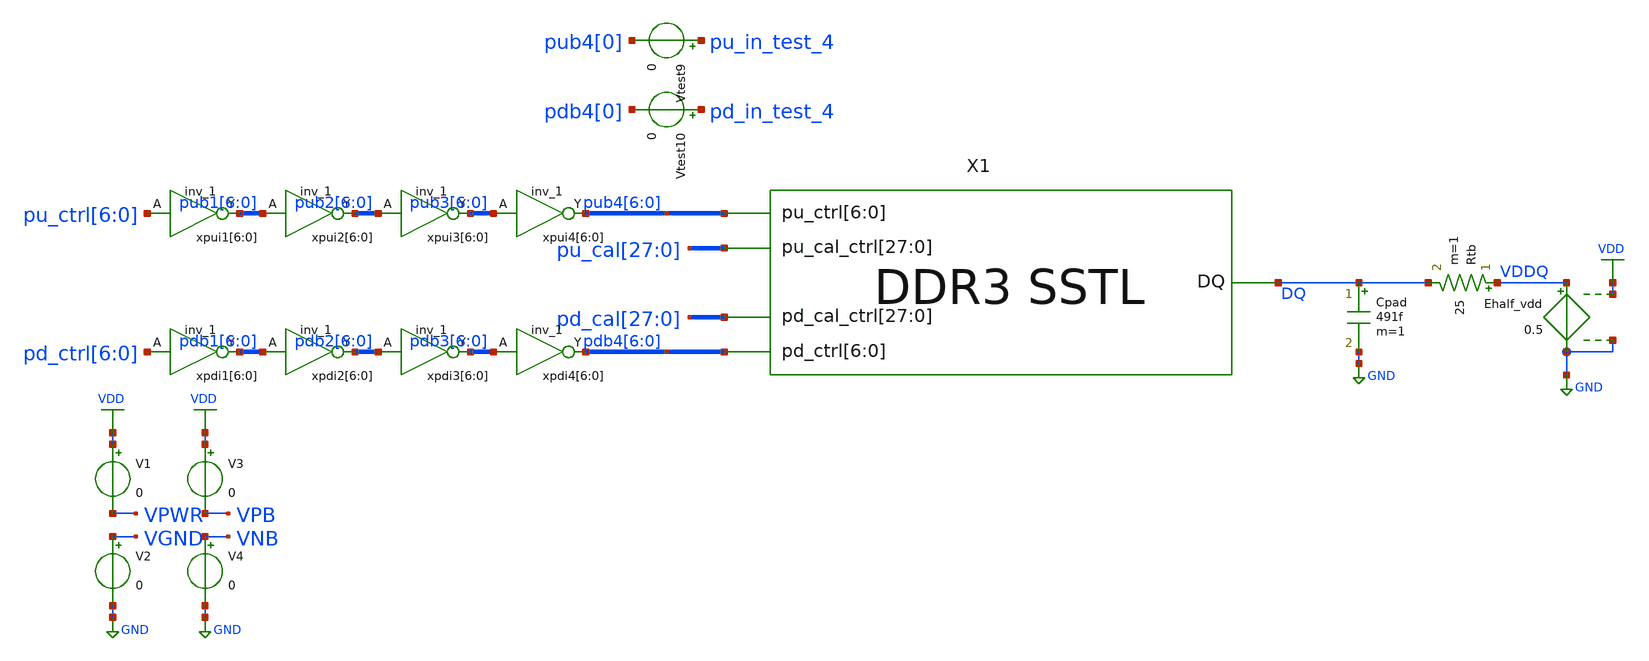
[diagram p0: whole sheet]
** sch_path: sstl_slew_tb.sch
* Copyright 2021 Stefan Frederik Schippers
* Licensed under the Apache License, Version 2.0 (the "License");
* you may not use this file except in compliance with the License.
* You may obtain a copy of the License at
* https://www.apache.org/licenses/LICENSE-2.0
* Unless required by applicable law or agreed to in writing, software
* distributed under the License is distributed on an "AS IS" BASIS,
* WITHOUT WARRANTIES OR CONDITIONS OF ANY KIND, either express or implied.
* See the License for the specific language governing permissions and
* limitations under the License.
**.subckt sstl_slew_tb
X1 DQ pdb4[6] pdb4[5] pdb4[4] pdb4[3] pdb4[2] pdb4[1] pdb4[0] pub4[6] pub4[5] pub4[4] pub4[3]
+ pub4[2] pub4[1] pub4[0] pd_cal[27] pd_cal[26] pd_cal[25] pd_cal[24] pd_cal[23] pd_cal[22] pd_cal[21]
+ pd_cal[20] pd_cal[19] pd_cal[18] pd_cal[17] pd_cal[16] pd_cal[15] pd_cal[14] pd_cal[13] pd_cal[12] pd_cal[11]
+ pd_cal[10] pd_cal[9] pd_cal[8] pd_cal[7] pd_cal[6] pd_cal[5] pd_cal[4] pd_cal[3] pd_cal[2] pd_cal[1] pd_cal[0]
+ pu_cal[27] pu_cal[26] pu_cal[25] pu_cal[24] pu_cal[23] pu_cal[22] pu_cal[21] pu_cal[20] pu_cal[19] pu_cal[18]
+ pu_cal[17] pu_cal[16] pu_cal[15] pu_cal[14] pu_cal[13] pu_cal[12] pu_cal[11] pu_cal[10] pu_cal[9] pu_cal[8]
+ pu_cal[7] pu_cal[6] pu_cal[5] pu_cal[4] pu_cal[3] pu_cal[2] pu_cal[1] pu_cal[0] SSTL
Rtb VDDQ DQ 25 m=1
Cpad DQ GND 491f m=1
Ehalf_vdd VDDQ GND VDD GND 0.5
xpui1[6] pu_ctrl[6] VGND VNB VPB VPWR pub1[6] sky130_fd_sc_hd__inv_1
xpui1[5] pu_ctrl[5] VGND VNB VPB VPWR pub1[5] sky130_fd_sc_hd__inv_1
xpui1[4] pu_ctrl[4] VGND VNB VPB VPWR pub1[4] sky130_fd_sc_hd__inv_1
xpui1[3] pu_ctrl[3] VGND VNB VPB VPWR pub1[3] sky130_fd_sc_hd__inv_1
xpui1[2] pu_ctrl[2] VGND VNB VPB VPWR pub1[2] sky130_fd_sc_hd__inv_1
xpui1[1] pu_ctrl[1] VGND VNB VPB VPWR pub1[1] sky130_fd_sc_hd__inv_1
xpui1[0] pu_ctrl[0] VGND VNB VPB VPWR pub1[0] sky130_fd_sc_hd__inv_1
xpui2[6] pub1[6] VGND VNB VPB VPWR pub2[6] sky130_fd_sc_hd__inv_1
xpui2[5] pub1[5] VGND VNB VPB VPWR pub2[5] sky130_fd_sc_hd__inv_1
xpui2[4] pub1[4] VGND VNB VPB VPWR pub2[4] sky130_fd_sc_hd__inv_1
xpui2[3] pub1[3] VGND VNB VPB VPWR pub2[3] sky130_fd_sc_hd__inv_1
xpui2[2] pub1[2] VGND VNB VPB VPWR pub2[2] sky130_fd_sc_hd__inv_1
xpui2[1] pub1[1] VGND VNB VPB VPWR pub2[1] sky130_fd_sc_hd__inv_1
xpui2[0] pub1[0] VGND VNB VPB VPWR pub2[0] sky130_fd_sc_hd__inv_1
xpui3[6] pub2[6] VGND VNB VPB VPWR pub3[6] sky130_fd_sc_hd__inv_1
xpui3[5] pub2[5] VGND VNB VPB VPWR pub3[5] sky130_fd_sc_hd__inv_1
xpui3[4] pub2[4] VGND VNB VPB VPWR pub3[4] sky130_fd_sc_hd__inv_1
xpui3[3] pub2[3] VGND VNB VPB VPWR pub3[3] sky130_fd_sc_hd__inv_1
xpui3[2] pub2[2] VGND VNB VPB VPWR pub3[2] sky130_fd_sc_hd__inv_1
xpui3[1] pub2[1] VGND VNB VPB VPWR pub3[1] sky130_fd_sc_hd__inv_1
xpui3[0] pub2[0] VGND VNB VPB VPWR pub3[0] sky130_fd_sc_hd__inv_1
xpui4[6] pub3[6] VGND VNB VPB VPWR pub4[6] sky130_fd_sc_hd__inv_1
xpui4[5] pub3[5] VGND VNB VPB VPWR pub4[5] sky130_fd_sc_hd__inv_1
xpui4[4] pub3[4] VGND VNB VPB VPWR pub4[4] sky130_fd_sc_hd__inv_1
xpui4[3] pub3[3] VGND VNB VPB VPWR pub4[3] sky130_fd_sc_hd__inv_1
xpui4[2] pub3[2] VGND VNB VPB VPWR pub4[2] sky130_fd_sc_hd__inv_1
xpui4[1] pub3[1] VGND VNB VPB VPWR pub4[1] sky130_fd_sc_hd__inv_1
xpui4[0] pub3[0] VGND VNB VPB VPWR pub4[0] sky130_fd_sc_hd__inv_1
xpdi1[6] pd_ctrl[6] VGND VNB VPB VPWR pdb1[6] sky130_fd_sc_hd__inv_1
xpdi1[5] pd_ctrl[5] VGND VNB VPB VPWR pdb1[5] sky130_fd_sc_hd__inv_1
xpdi1[4] pd_ctrl[4] VGND VNB VPB VPWR pdb1[4] sky130_fd_sc_hd__inv_1
xpdi1[3] pd_ctrl[3] VGND VNB VPB VPWR pdb1[3] sky130_fd_sc_hd__inv_1
xpdi1[2] pd_ctrl[2] VGND VNB VPB VPWR pdb1[2] sky130_fd_sc_hd__inv_1
xpdi1[1] pd_ctrl[1] VGND VNB VPB VPWR pdb1[1] sky130_fd_sc_hd__inv_1
xpdi1[0] pd_ctrl[0] VGND VNB VPB VPWR pdb1[0] sky130_fd_sc_hd__inv_1
xpdi2[6] pdb1[6] VGND VNB VPB VPWR pdb2[6] sky130_fd_sc_hd__inv_1
xpdi2[5] pdb1[5] VGND VNB VPB VPWR pdb2[5] sky130_fd_sc_hd__inv_1
xpdi2[4] pdb1[4] VGND VNB VPB VPWR pdb2[4] sky130_fd_sc_hd__inv_1
xpdi2[3] pdb1[3] VGND VNB VPB VPWR pdb2[3] sky130_fd_sc_hd__inv_1
xpdi2[2] pdb1[2] VGND VNB VPB VPWR pdb2[2] sky130_fd_sc_hd__inv_1
xpdi2[1] pdb1[1] VGND VNB VPB VPWR pdb2[1] sky130_fd_sc_hd__inv_1
xpdi2[0] pdb1[0] VGND VNB VPB VPWR pdb2[0] sky130_fd_sc_hd__inv_1
xpdi3[6] pdb2[6] VGND VNB VPB VPWR pdb3[6] sky130_fd_sc_hd__inv_1
xpdi3[5] pdb2[5] VGND VNB VPB VPWR pdb3[5] sky130_fd_sc_hd__inv_1
xpdi3[4] pdb2[4] VGND VNB VPB VPWR pdb3[4] sky130_fd_sc_hd__inv_1
xpdi3[3] pdb2[3] VGND VNB VPB VPWR pdb3[3] sky130_fd_sc_hd__inv_1
xpdi3[2] pdb2[2] VGND VNB VPB VPWR pdb3[2] sky130_fd_sc_hd__inv_1
xpdi3[1] pdb2[1] VGND VNB VPB VPWR pdb3[1] sky130_fd_sc_hd__inv_1
xpdi3[0] pdb2[0] VGND VNB VPB VPWR pdb3[0] sky130_fd_sc_hd__inv_1
xpdi4[6] pdb3[6] VGND VNB VPB VPWR pdb4[6] sky130_fd_sc_hd__inv_1
xpdi4[5] pdb3[5] VGND VNB VPB VPWR pdb4[5] sky130_fd_sc_hd__inv_1
xpdi4[4] pdb3[4] VGND VNB VPB VPWR pdb4[4] sky130_fd_sc_hd__inv_1
xpdi4[3] pdb3[3] VGND VNB VPB VPWR pdb4[3] sky130_fd_sc_hd__inv_1
xpdi4[2] pdb3[2] VGND VNB VPB VPWR pdb4[2] sky130_fd_sc_hd__inv_1
xpdi4[1] pdb3[1] VGND VNB VPB VPWR pdb4[1] sky130_fd_sc_hd__inv_1
xpdi4[0] pdb3[0] VGND VNB VPB VPWR pdb4[0] sky130_fd_sc_hd__inv_1
V1 VDD VPWR 0
V2 VGND GND 0
V3 VDD VPB 0
V4 VNB GND 0
Vtest9 pu_in_test_4 pub4[0] 0
Vtest10 pd_in_test_4 pdb4[0] 0
**** begin user architecture code
 ** Local library links to pdk
.lib ./libs/SED_process_SED_lib.spice SED_process_SED
.include $::SKYWATER_STDCELLS/sky130_fd_sc_hd.spice

**** end user architecture code
**.ends

* expanding   symbol:  SSTL.sym # of pins=5
** sym_path: SSTL.sym
** sch_path: SSTL.sch
.subckt SSTL DQ pd_ctrl[6] pd_ctrl[5] pd_ctrl[4] pd_ctrl[3] pd_ctrl[2] pd_ctrl[1] pd_ctrl[0]
+ pu_ctrl[6] pu_ctrl[5] pu_ctrl[4] pu_ctrl[3] pu_ctrl[2] pu_ctrl[1] pu_ctrl[0] pd_cal_ctrl[27] pd_cal_ctrl[26]
+ pd_cal_ctrl[25] pd_cal_ctrl[24] pd_cal_ctrl[23] pd_cal_ctrl[22] pd_cal_ctrl[21] pd_cal_ctrl[20] pd_cal_ctrl[19]
+ pd_cal_ctrl[18] pd_cal_ctrl[17] pd_cal_ctrl[16] pd_cal_ctrl[15] pd_cal_ctrl[14] pd_cal_ctrl[13] pd_cal_ctrl[12]
+ pd_cal_ctrl[11] pd_cal_ctrl[10] pd_cal_ctrl[9] pd_cal_ctrl[8] pd_cal_ctrl[7] pd_cal_ctrl[6] pd_cal_ctrl[5]
+ pd_cal_ctrl[4] pd_cal_ctrl[3] pd_cal_ctrl[2] pd_cal_ctrl[1] pd_cal_ctrl[0] pu_cal_ctrl[27] pu_cal_ctrl[26]
+ pu_cal_ctrl[25] pu_cal_ctrl[24] pu_cal_ctrl[23] pu_cal_ctrl[22] pu_cal_ctrl[21] pu_cal_ctrl[20] pu_cal_ctrl[19]
+ pu_cal_ctrl[18] pu_cal_ctrl[17] pu_cal_ctrl[16] pu_cal_ctrl[15] pu_cal_ctrl[14] pu_cal_ctrl[13] pu_cal_ctrl[12]
+ pu_cal_ctrl[11] pu_cal_ctrl[10] pu_cal_ctrl[9] pu_cal_ctrl[8] pu_cal_ctrl[7] pu_cal_ctrl[6] pu_cal_ctrl[5]
+ pu_cal_ctrl[4] pu_cal_ctrl[3] pu_cal_ctrl[2] pu_cal_ctrl[1] pu_cal_ctrl[0]
*.iopin DQ
*.ipin
*+ pu_cal_ctrl[27],pu_cal_ctrl[26],pu_cal_ctrl[25],pu_cal_ctrl[24],pu_cal_ctrl[23],pu_cal_ctrl[22],pu_cal_ctrl[21],pu_cal_ctrl[20],pu_cal_ctrl[19],pu_cal_ctrl[18],pu_cal_ctrl[17],pu_cal_ctrl[16],pu_cal_ctrl[15],pu_cal_ctrl[14],pu_cal_ctrl[13],pu_cal_ctrl[12],pu_cal_ctrl[11],pu_cal_ctrl[10],pu_cal_ctrl[9],pu_cal_ctrl[8],pu_cal_ctrl[7],pu_cal_ctrl[6],pu_cal_ctrl[5],pu_cal_ctrl[4],pu_cal_ctrl[3],pu_cal_ctrl[2],pu_cal_ctrl[1],pu_cal_ctrl[0]
*.ipin
*+ pd_cal_ctrl[27],pd_cal_ctrl[26],pd_cal_ctrl[25],pd_cal_ctrl[24],pd_cal_ctrl[23],pd_cal_ctrl[22],pd_cal_ctrl[21],pd_cal_ctrl[20],pd_cal_ctrl[19],pd_cal_ctrl[18],pd_cal_ctrl[17],pd_cal_ctrl[16],pd_cal_ctrl[15],pd_cal_ctrl[14],pd_cal_ctrl[13],pd_cal_ctrl[12],pd_cal_ctrl[11],pd_cal_ctrl[10],pd_cal_ctrl[9],pd_cal_ctrl[8],pd_cal_ctrl[7],pd_cal_ctrl[6],pd_cal_ctrl[5],pd_cal_ctrl[4],pd_cal_ctrl[3],pd_cal_ctrl[2],pd_cal_ctrl[1],pd_cal_ctrl[0]
*.ipin pu_ctrl[6],pu_ctrl[5],pu_ctrl[4],pu_ctrl[3],pu_ctrl[2],pu_ctrl[1],pu_ctrl[0]
*.ipin pd_ctrl[6],pd_ctrl[5],pd_ctrl[4],pd_ctrl[3],pd_ctrl[2],pd_ctrl[1],pd_ctrl[0]
X1 DQ n_pu_ctrl[6] n_pu_cal_ctrl[27] n_pu_cal_ctrl[26] n_pu_cal_ctrl[25] n_pu_cal_ctrl[24] p-leg
X2 DQ pd_ctrl_buff[6] pd_cal_ctrl[27] pd_cal_ctrl[26] pd_cal_ctrl[25] pd_cal_ctrl[24] n-leg
X3 DQ n_pu_ctrl[5] n_pu_cal_ctrl[23] n_pu_cal_ctrl[22] n_pu_cal_ctrl[21] n_pu_cal_ctrl[20] p-leg
X4 DQ pd_ctrl_buff[5] pd_cal_ctrl[23] pd_cal_ctrl[22] pd_cal_ctrl[21] pd_cal_ctrl[20] n-leg
X5 DQ n_pu_ctrl[4] n_pu_cal_ctrl[19] n_pu_cal_ctrl[18] n_pu_cal_ctrl[17] n_pu_cal_ctrl[16] p-leg
X6 DQ pd_ctrl_buff[4] pd_cal_ctrl[19] pd_cal_ctrl[18] pd_cal_ctrl[17] pd_cal_ctrl[16] n-leg
X7 DQ n_pu_ctrl[3] n_pu_cal_ctrl[15] n_pu_cal_ctrl[14] n_pu_cal_ctrl[13] n_pu_cal_ctrl[12] p-leg
X8 DQ pd_ctrl_buff[3] pd_cal_ctrl[15] pd_cal_ctrl[14] pd_cal_ctrl[13] pd_cal_ctrl[12] n-leg
X9 DQ n_pu_ctrl[2] n_pu_cal_ctrl[11] n_pu_cal_ctrl[10] n_pu_cal_ctrl[9] n_pu_cal_ctrl[8] p-leg
X10 DQ pd_ctrl_buff[2] pd_cal_ctrl[11] pd_cal_ctrl[10] pd_cal_ctrl[9] pd_cal_ctrl[8] n-leg
X11 DQ n_pu_ctrl[1] n_pu_cal_ctrl[7] n_pu_cal_ctrl[6] n_pu_cal_ctrl[5] n_pu_cal_ctrl[4] p-leg
X12 DQ pd_ctrl_buff[1] pd_cal_ctrl[7] pd_cal_ctrl[6] pd_cal_ctrl[5] pd_cal_ctrl[4] n-leg
X13 DQ n_pu_ctrl[0] n_pu_cal_ctrl[3] n_pu_cal_ctrl[2] n_pu_cal_ctrl[1] n_pu_cal_ctrl[0] p-leg
X14 DQ pd_ctrl_buff[0] pd_cal_ctrl[3] pd_cal_ctrl[2] pd_cal_ctrl[1] pd_cal_ctrl[0] n-leg
xpd_buff_4[6] pd_ctrl[6] VGND VNB VPB VPWR pdc4[6] sky130_fd_sc_hd__inv_4
xpd_buff_4[5] pd_ctrl[5] VGND VNB VPB VPWR pdc4[5] sky130_fd_sc_hd__inv_4
xpd_buff_4[4] pd_ctrl[4] VGND VNB VPB VPWR pdc4[4] sky130_fd_sc_hd__inv_4
xpd_buff_4[3] pd_ctrl[3] VGND VNB VPB VPWR pdc4[3] sky130_fd_sc_hd__inv_4
xpd_buff_4[2] pd_ctrl[2] VGND VNB VPB VPWR pdc4[2] sky130_fd_sc_hd__inv_4
xpd_buff_4[1] pd_ctrl[1] VGND VNB VPB VPWR pdc4[1] sky130_fd_sc_hd__inv_4
xpd_buff_4[0] pd_ctrl[0] VGND VNB VPB VPWR pdc4[0] sky130_fd_sc_hd__inv_4
xpd_buff_6[6] pdc4[6] VGND VNB VPB VPWR pd_ctrl_buff[6] sky130_fd_sc_hd__inv_6
xpd_buff_6[5] pdc4[5] VGND VNB VPB VPWR pd_ctrl_buff[5] sky130_fd_sc_hd__inv_6
xpd_buff_6[4] pdc4[4] VGND VNB VPB VPWR pd_ctrl_buff[4] sky130_fd_sc_hd__inv_6
xpd_buff_6[3] pdc4[3] VGND VNB VPB VPWR pd_ctrl_buff[3] sky130_fd_sc_hd__inv_6
xpd_buff_6[2] pdc4[2] VGND VNB VPB VPWR pd_ctrl_buff[2] sky130_fd_sc_hd__inv_6
xpd_buff_6[1] pdc4[1] VGND VNB VPB VPWR pd_ctrl_buff[1] sky130_fd_sc_hd__inv_6
xpd_buff_6[0] pdc4[0] VGND VNB VPB VPWR pd_ctrl_buff[0] sky130_fd_sc_hd__inv_6
xpu_buff_4[6] puc1[6] VGND VNB VPB VPWR puc4[6] sky130_fd_sc_hd__inv_4
xpu_buff_4[5] puc1[5] VGND VNB VPB VPWR puc4[5] sky130_fd_sc_hd__inv_4
xpu_buff_4[4] puc1[4] VGND VNB VPB VPWR puc4[4] sky130_fd_sc_hd__inv_4
xpu_buff_4[3] puc1[3] VGND VNB VPB VPWR puc4[3] sky130_fd_sc_hd__inv_4
xpu_buff_4[2] puc1[2] VGND VNB VPB VPWR puc4[2] sky130_fd_sc_hd__inv_4
xpu_buff_4[1] puc1[1] VGND VNB VPB VPWR puc4[1] sky130_fd_sc_hd__inv_4
xpu_buff_4[0] puc1[0] VGND VNB VPB VPWR puc4[0] sky130_fd_sc_hd__inv_4
xpu_buff_6[6] puc4[6] VGND VNB VPB VPWR n_pu_ctrl[6] sky130_fd_sc_hd__inv_6
xpu_buff_6[5] puc4[5] VGND VNB VPB VPWR n_pu_ctrl[5] sky130_fd_sc_hd__inv_6
xpu_buff_6[4] puc4[4] VGND VNB VPB VPWR n_pu_ctrl[4] sky130_fd_sc_hd__inv_6
xpu_buff_6[3] puc4[3] VGND VNB VPB VPWR n_pu_ctrl[3] sky130_fd_sc_hd__inv_6
xpu_buff_6[2] puc4[2] VGND VNB VPB VPWR n_pu_ctrl[2] sky130_fd_sc_hd__inv_6
xpu_buff_6[1] puc4[1] VGND VNB VPB VPWR n_pu_ctrl[1] sky130_fd_sc_hd__inv_6
xpu_buff_6[0] puc4[0] VGND VNB VPB VPWR n_pu_ctrl[0] sky130_fd_sc_hd__inv_6
xpu_buff_1[6] pu_ctrl[6] VGND VNB VPB VPWR puc1[6] sky130_fd_sc_hd__inv_1
xpu_buff_1[5] pu_ctrl[5] VGND VNB VPB VPWR puc1[5] sky130_fd_sc_hd__inv_1
xpu_buff_1[4] pu_ctrl[4] VGND VNB VPB VPWR puc1[4] sky130_fd_sc_hd__inv_1
xpu_buff_1[3] pu_ctrl[3] VGND VNB VPB VPWR puc1[3] sky130_fd_sc_hd__inv_1
xpu_buff_1[2] pu_ctrl[2] VGND VNB VPB VPWR puc1[2] sky130_fd_sc_hd__inv_1
xpu_buff_1[1] pu_ctrl[1] VGND VNB VPB VPWR puc1[1] sky130_fd_sc_hd__inv_1
xpu_buff_1[0] pu_ctrl[0] VGND VNB VPB VPWR puc1[0] sky130_fd_sc_hd__inv_1
xpu_cal_inv[27] pu_cal_ctrl[27] VGND VNB VPB VPWR n_pu_cal_ctrl[27] sky130_fd_sc_hd__inv_1
xpu_cal_inv[26] pu_cal_ctrl[26] VGND VNB VPB VPWR n_pu_cal_ctrl[26] sky130_fd_sc_hd__inv_1
xpu_cal_inv[25] pu_cal_ctrl[25] VGND VNB VPB VPWR n_pu_cal_ctrl[25] sky130_fd_sc_hd__inv_1
xpu_cal_inv[24] pu_cal_ctrl[24] VGND VNB VPB VPWR n_pu_cal_ctrl[24] sky130_fd_sc_hd__inv_1
xpu_cal_inv[23] pu_cal_ctrl[23] VGND VNB VPB VPWR n_pu_cal_ctrl[23] sky130_fd_sc_hd__inv_1
xpu_cal_inv[22] pu_cal_ctrl[22] VGND VNB VPB VPWR n_pu_cal_ctrl[22] sky130_fd_sc_hd__inv_1
xpu_cal_inv[21] pu_cal_ctrl[21] VGND VNB VPB VPWR n_pu_cal_ctrl[21] sky130_fd_sc_hd__inv_1
xpu_cal_inv[20] pu_cal_ctrl[20] VGND VNB VPB VPWR n_pu_cal_ctrl[20] sky130_fd_sc_hd__inv_1
xpu_cal_inv[19] pu_cal_ctrl[19] VGND VNB VPB VPWR n_pu_cal_ctrl[19] sky130_fd_sc_hd__inv_1
xpu_cal_inv[18] pu_cal_ctrl[18] VGND VNB VPB VPWR n_pu_cal_ctrl[18] sky130_fd_sc_hd__inv_1
xpu_cal_inv[17] pu_cal_ctrl[17] VGND VNB VPB VPWR n_pu_cal_ctrl[17] sky130_fd_sc_hd__inv_1
xpu_cal_inv[16] pu_cal_ctrl[16] VGND VNB VPB VPWR n_pu_cal_ctrl[16] sky130_fd_sc_hd__inv_1
xpu_cal_inv[15] pu_cal_ctrl[15] VGND VNB VPB VPWR n_pu_cal_ctrl[15] sky130_fd_sc_hd__inv_1
xpu_cal_inv[14] pu_cal_ctrl[14] VGND VNB VPB VPWR n_pu_cal_ctrl[14] sky130_fd_sc_hd__inv_1
xpu_cal_inv[13] pu_cal_ctrl[13] VGND VNB VPB VPWR n_pu_cal_ctrl[13] sky130_fd_sc_hd__inv_1
xpu_cal_inv[12] pu_cal_ctrl[12] VGND VNB VPB VPWR n_pu_cal_ctrl[12] sky130_fd_sc_hd__inv_1
xpu_cal_inv[11] pu_cal_ctrl[11] VGND VNB VPB VPWR n_pu_cal_ctrl[11] sky130_fd_sc_hd__inv_1
xpu_cal_inv[10] pu_cal_ctrl[10] VGND VNB VPB VPWR n_pu_cal_ctrl[10] sky130_fd_sc_hd__inv_1
xpu_cal_inv[9] pu_cal_ctrl[9] VGND VNB VPB VPWR n_pu_cal_ctrl[9] sky130_fd_sc_hd__inv_1
xpu_cal_inv[8] pu_cal_ctrl[8] VGND VNB VPB VPWR n_pu_cal_ctrl[8] sky130_fd_sc_hd__inv_1
xpu_cal_inv[7] pu_cal_ctrl[7] VGND VNB VPB VPWR n_pu_cal_ctrl[7] sky130_fd_sc_hd__inv_1
xpu_cal_inv[6] pu_cal_ctrl[6] VGND VNB VPB VPWR n_pu_cal_ctrl[6] sky130_fd_sc_hd__inv_1
xpu_cal_inv[5] pu_cal_ctrl[5] VGND VNB VPB VPWR n_pu_cal_ctrl[5] sky130_fd_sc_hd__inv_1
xpu_cal_inv[4] pu_cal_ctrl[4] VGND VNB VPB VPWR n_pu_cal_ctrl[4] sky130_fd_sc_hd__inv_1
xpu_cal_inv[3] pu_cal_ctrl[3] VGND VNB VPB VPWR n_pu_cal_ctrl[3] sky130_fd_sc_hd__inv_1
xpu_cal_inv[2] pu_cal_ctrl[2] VGND VNB VPB VPWR n_pu_cal_ctrl[2] sky130_fd_sc_hd__inv_1
xpu_cal_inv[1] pu_cal_ctrl[1] VGND VNB VPB VPWR n_pu_cal_ctrl[1] sky130_fd_sc_hd__inv_1
xpu_cal_inv[0] pu_cal_ctrl[0] VGND VNB VPB VPWR n_pu_cal_ctrl[0] sky130_fd_sc_hd__inv_1
V1 VDD VPWR 0
V2 VGND GND 0
V3 VDD VPB 0
V4 VNB GND 0
.ends


* expanding   symbol:  p-leg.sym # of pins=3
** sym_path: p-leg.sym
** sch_path: p-leg.sch
.subckt p-leg DQ n_pu_ctrl n_cal_ctrl[3] n_cal_ctrl[2] n_cal_ctrl[1] n_cal_ctrl[0]
*.ipin n_cal_ctrl[3],n_cal_ctrl[2],n_cal_ctrl[1],n_cal_ctrl[0]
*.ipin n_pu_ctrl
*.iopin DQ
XR1 DQ net1 sky130_fd_pr__res_generic_po W=0.33 L=1.8 m=1
XMpullup net1 n_pu_ctrl VDD VDD sky130_fd_pr__pfet_01v8_lvt L=0.35 W=1 nf=1 ad='int((nf+1)/2) * W/nf * 0.29'
+ as='int((nf+2)/2) * W/nf * 0.29' pd='2*int((nf+1)/2) * (W/nf + 0.29)' ps='2*int((nf+2)/2) * (W/nf + 0.29)'
+ nrd='0.29 / W' nrs='0.29 / W' sa=0 sb=0 sd=0 mult=128 m=128
XMctrltot VDD n_cal_ctrl[0] VDD VDD sky130_fd_pr__pfet_01v8_lvt L=0.35 W=1 nf=1 ad='int((nf+1)/2) * W/nf * 0.29'
+ as='int((nf+2)/2) * W/nf * 0.29' pd='2*int((nf+1)/2) * (W/nf + 0.29)' ps='2*int((nf+2)/2) * (W/nf + 0.29)'
+ nrd='0.29 / W' nrs='0.29 / W' sa=0 sb=0 sd=0 mult=120 m=120
XMctrl0 DQ n_cal_ctrl[0] net1 VDD sky130_fd_pr__pfet_01v8_lvt L=0.35 W=1 nf=1 ad='int((nf+1)/2) * W/nf * 0.29'
+ as='int((nf+2)/2) * W/nf * 0.29' pd='2*int((nf+1)/2) * (W/nf + 0.29)' ps='2*int((nf+2)/2) * (W/nf + 0.29)'
+ nrd='0.29 / W' nrs='0.29 / W' sa=0 sb=0 sd=0 mult=48 m=48
XMctrl1 DQ n_cal_ctrl[1] net1 VDD sky130_fd_pr__pfet_01v8_lvt L=0.35 W=1 nf=1 ad='int((nf+1)/2) * W/nf * 0.29'
+ as='int((nf+2)/2) * W/nf * 0.29' pd='2*int((nf+1)/2) * (W/nf + 0.29)' ps='2*int((nf+2)/2) * (W/nf + 0.29)'
+ nrd='0.29 / W' nrs='0.29 / W' sa=0 sb=0 sd=0 mult=16 m=16
XMctrl2 DQ n_cal_ctrl[2] net1 VDD sky130_fd_pr__pfet_01v8_lvt L=0.35 W=1 nf=1 ad='int((nf+1)/2) * W/nf * 0.29'
+ as='int((nf+2)/2) * W/nf * 0.29' pd='2*int((nf+1)/2) * (W/nf + 0.29)' ps='2*int((nf+2)/2) * (W/nf + 0.29)'
+ nrd='0.29 / W' nrs='0.29 / W' sa=0 sb=0 sd=0 mult=8 m=8
XMctrl3 DQ n_cal_ctrl[3] net1 VDD sky130_fd_pr__pfet_01v8_lvt L=0.35 W=1 nf=1 ad='int((nf+1)/2) * W/nf * 0.29'
+ as='int((nf+2)/2) * W/nf * 0.29' pd='2*int((nf+1)/2) * (W/nf + 0.29)' ps='2*int((nf+2)/2) * (W/nf + 0.29)'
+ nrd='0.29 / W' nrs='0.29 / W' sa=0 sb=0 sd=0 mult=4 m=4
.ends


* expanding   symbol:  n-leg.sym # of pins=3
** sym_path: schem/n-leg.sym
** sch_path: schem/n-leg.sch
.subckt n-leg DQ pd_ctrl cal_ctrl[3] cal_ctrl[2] cal_ctrl[1] cal_ctrl[0]
*.iopin DQ
*.ipin pd_ctrl
*.ipin cal_ctrl[3],cal_ctrl[2],cal_ctrl[1],cal_ctrl[0]
XR1 vpulldown net1 sky130_fd_pr__res_generic_po W=0.33 L=1.7 m=1
Xn1 vpulldown net2 GND GND sky130_fd_pr__nfet_01v8 L=0.15 W=0.65 nf=1 ad='int((nf+1)/2) * W/nf * 0.29'
+ as='int((nf+2)/2) * W/nf * 0.29' pd='2*int((nf+1)/2) * (W/nf + 0.29)' ps='2*int((nf+2)/2) * (W/nf + 0.29)'
+ nrd='0.29 / W' nrs='0.29 / W' sa=0 sb=0 sd=0 mult=48 m=48
Xnctrl0 net1 cal_ctrl[0] vpulldown GND sky130_fd_pr__nfet_01v8 L=0.15 W=0.65 nf=1 ad='int((nf+1)/2) * W/nf * 0.29'
+ as='int((nf+2)/2) * W/nf * 0.29' pd='2*int((nf+1)/2) * (W/nf + 0.29)' ps='2*int((nf+2)/2) * (W/nf + 0.29)'
+ nrd='0.29 / W' nrs='0.29 / W' sa=0 sb=0 sd=0 mult=32 m=32
Xnctrl1 net1 cal_ctrl[1] vpulldown GND sky130_fd_pr__nfet_01v8 L=0.15 W=0.65 nf=1 ad='int((nf+1)/2) * W/nf * 0.29'
+ as='int((nf+2)/2) * W/nf * 0.29' pd='2*int((nf+1)/2) * (W/nf + 0.29)' ps='2*int((nf+2)/2) * (W/nf + 0.29)'
+ nrd='0.29 / W' nrs='0.29 / W' sa=0 sb=0 sd=0 mult=8 m=8
Xnctrl2 net1 cal_ctrl[2] vpulldown GND sky130_fd_pr__nfet_01v8 L=0.15 W=0.975 nf=1 ad='int((nf+1)/2) * W/nf * 0.29'
+ as='int((nf+2)/2) * W/nf * 0.29' pd='2*int((nf+1)/2) * (W/nf + 0.29)' ps='2*int((nf+2)/2) * (W/nf + 0.29)'
+ nrd='0.29 / W' nrs='0.29 / W' sa=0 sb=0 sd=0 mult=2 m=2
Xnctrl3 net1 cal_ctrl[3] vpulldown GND sky130_fd_pr__nfet_01v8 L=0.15 W=0.5 nf=1 ad='int((nf+1)/2) * W/nf * 0.29'
+ as='int((nf+2)/2) * W/nf * 0.29' pd='2*int((nf+1)/2) * (W/nf + 0.29)' ps='2*int((nf+2)/2) * (W/nf + 0.29)'
+ nrd='0.29 / W' nrs='0.29 / W' sa=0 sb=0 sd=0 mult=1 m=1
Xnctrl_tot GND GND GND GND sky130_fd_pr__nfet_01v8 L=0.15 W=0.65 nf=1 ad='int((nf+1)/2) * W/nf * 0.29'
+ as='int((nf+2)/2) * W/nf * 0.29' pd='2*int((nf+1)/2) * (W/nf + 0.29)' ps='2*int((nf+2)/2) * (W/nf + 0.29)'
+ nrd='0.29 / W' nrs='0.29 / W' sa=0 sb=0 sd=0 mult=11 m=11
Vcur_out DQ net1 0
.save i(vcur_out)
Vcur_in pd_ctrl net2 0
.save i(vcur_in)
.ends

.GLOBAL GND
.GLOBAL VDD
**** begin user architecture code


* power voltage
vvdd VDD 0 SED_vdd_SED

** CALIBRATION CONTROL **
* PULLUP
vpu_cal00 pu_cal[0] 0 SED_pucal00_SED
vpu_cal01 pu_cal[1] 0 SED_pucal01_SED
vpu_cal02 pu_cal[2] 0 SED_pucal02_SED
vpu_cal03 pu_cal[3] 0 SED_pucal03_SED
vpu_cal10 pu_cal[4] 0 SED_pucal10_SED
vpu_cal11 pu_cal[5] 0 SED_pucal11_SED
vpu_cal12 pu_cal[6] 0 SED_pucal12_SED
vpu_cal13 pu_cal[7] 0 SED_pucal13_SED
vpu_cal20 pu_cal[8] 0 SED_pucal20_SED
vpu_cal21 pu_cal[9] 0 SED_pucal21_SED
vpu_cal22 pu_cal[10] 0 SED_pucal22_SED
vpu_cal23 pu_cal[11] 0 SED_pucal23_SED
vpu_cal30 pu_cal[12] 0 SED_pucal30_SED
vpu_cal31 pu_cal[13] 0 SED_pucal31_SED
vpu_cal32 pu_cal[14] 0 SED_pucal32_SED
vpu_cal33 pu_cal[15] 0 SED_pucal33_SED
vpu_cal40 pu_cal[16] 0 SED_pucal40_SED
vpu_cal41 pu_cal[17] 0 SED_pucal41_SED
vpu_cal42 pu_cal[18] 0 SED_pucal42_SED
vpu_cal43 pu_cal[19] 0 SED_pucal43_SED
vpu_cal50 pu_cal[20] 0 SED_pucal50_SED
vpu_cal51 pu_cal[21] 0 SED_pucal51_SED
vpu_cal52 pu_cal[22] 0 SED_pucal52_SED
vpu_cal53 pu_cal[23] 0 SED_pucal53_SED
vpu_cal60 pu_cal[24] 0 SED_pucal60_SED
vpu_cal61 pu_cal[25] 0 SED_pucal61_SED
vpu_cal62 pu_cal[26] 0 SED_pucal62_SED
vpu_cal63 pu_cal[27] 0 SED_pucal63_SED
* PULLDOWN
vpd_cal00 pd_cal[0] 0 SED_pdcal00_SED
vpd_cal01 pd_cal[1] 0 SED_pdcal01_SED
vpd_cal02 pd_cal[2] 0 SED_pdcal02_SED
vpd_cal03 pd_cal[3] 0 SED_pdcal03_SED
vpd_cal10 pd_cal[4] 0 SED_pdcal10_SED
vpd_cal11 pd_cal[5] 0 SED_pdcal11_SED
vpd_cal12 pd_cal[6] 0 SED_pdcal12_SED
vpd_cal13 pd_cal[7] 0 SED_pdcal13_SED
vpd_cal20 pd_cal[8] 0 SED_pdcal20_SED
vpd_cal21 pd_cal[9] 0 SED_pdcal21_SED
vpd_cal22 pd_cal[10] 0 SED_pdcal22_SED
vpd_cal23 pd_cal[11] 0 SED_pdcal23_SED
vpd_cal30 pd_cal[12] 0 SED_pdcal30_SED
vpd_cal31 pd_cal[13] 0 SED_pdcal31_SED
vpd_cal32 pd_cal[14] 0 SED_pdcal32_SED
vpd_cal33 pd_cal[15] 0 SED_pdcal33_SED
vpd_cal40 pd_cal[16] 0 SED_pdcal40_SED
vpd_cal41 pd_cal[17] 0 SED_pdcal41_SED
vpd_cal42 pd_cal[18] 0 SED_pdcal42_SED
vpd_cal43 pd_cal[19] 0 SED_pdcal43_SED
vpd_cal50 pd_cal[20] 0 SED_pdcal50_SED
vpd_cal51 pd_cal[21] 0 SED_pdcal51_SED
vpd_cal52 pd_cal[22] 0 SED_pdcal52_SED
vpd_cal53 pd_cal[23] 0 SED_pdcal53_SED
vpd_cal60 pd_cal[24] 0 SED_pdcal60_SED
vpd_cal61 pd_cal[25] 0 SED_pdcal61_SED
vpd_cal62 pd_cal[26] 0 SED_pdcal62_SED
vpd_cal63 pd_cal[27] 0 SED_pdcal63_SED

** LEG ENABLE/DISABLE CONTROL
* PULLUP
vpu_ctrl0 pu_ctrl[0] 0 0 PULSE 0 SED_puctrl0_SED 10n 10p 10p 10n 20n 0
vpu_ctrl1 pu_ctrl[1] 0 0 PULSE 0 SED_puctrl1_SED 10n 10p 10p 10n 20n 0
vpu_ctrl2 pu_ctrl[2] 0 0 PULSE 0 SED_puctrl2_SED 10n 10p 10p 10n 20n 0
vpu_ctrl3 pu_ctrl[3] 0 0 PULSE 0 SED_puctrl3_SED 10n 10p 10p 10n 20n 0
vpu_ctrl4 pu_ctrl[4] 0 0 PULSE 0 SED_puctrl4_SED 10n 10p 10p 10n 20n 0
vpu_ctrl5 pu_ctrl[5] 0 0 PULSE 0 SED_puctrl5_SED 10n 10p 10p 10n 20n 0
vpu_ctrl6 pu_ctrl[6] 0 0 PULSE 0 SED_puctrl6_SED 10n 10p 10p 10n 20n 0
* PULLDOWN
vpd_ctrl0 VDD pd_ctrl[0] 0 PULSE 0 SED_pdctrl0_SED 10n 10p 10p 10n 20n 0
vpd_ctrl1 VDD pd_ctrl[1] 0 PULSE 0 SED_pdctrl1_SED 10n 10p 10p 10n 20n 0
vpd_ctrl2 VDD pd_ctrl[2] 0 PULSE 0 SED_pdctrl2_SED 10n 10p 10p 10n 20n 0
vpd_ctrl3 VDD pd_ctrl[3] 0 PULSE 0 SED_pdctrl3_SED 10n 10p 10p 10n 20n 0
vpd_ctrl4 VDD pd_ctrl[4] 0 PULSE 0 SED_pdctrl4_SED 10n 10p 10p 10n 20n 0
vpd_ctrl5 VDD pd_ctrl[5] 0 PULSE 0 SED_pdctrl5_SED 10n 10p 10p 10n 20n 0
vpd_ctrl6 VDD pd_ctrl[6] 0 PULSE 0 SED_pdctrl6_SED 10n 10p 10p 10n 20n 0

* Set V-out-low-AC and V-out-high-AC voltages
Evohac vohac 0 VDD 0 0.6
Evlhac volac 0 VDD 0 0.4

.control
set num_threads=4
save all
set temp=SED_temp_SED

* RUN SIMULATION
tran 1p 25n
* Measure rise time
*meas tran tdiff_rise trig dq val=volac rise=1 targ dq val=vohac rise=1
meas tran tdiff_rise trig dq val=SED_volac_SED rise=1 targ dq val=SED_vohac_SED rise=1
* Measure fall time
*meas tran tdiff_fall trig dq val=vohac fall=1 targ dq val=volac fall=1
meas tran tdiff_fall trig dq val=SED_vohac_SED fall=1 targ dq val=SED_volac_SED fall=1

* OUTPUT

wrdata ./out/data/SED_plotName_SED.txt tdiff_rise tdiff_fall
set hcopydevtype = svg
hardcopy ./out/plots/SED_plotName_SED.svg dq pu_in_test_4 pd_in_test_4 title 'DQ vs time'

*print i(vtest)
*wrdata out/data/SED_plotName_SED.txt i(vtest)
*set hcopydevtype = svg
*hardcopy ./out/plots/SED_plotName_SED.svg I(vtest) vs vddq title 'Resistance vs pin voltage'

.endc


**** end user architecture code
.end
